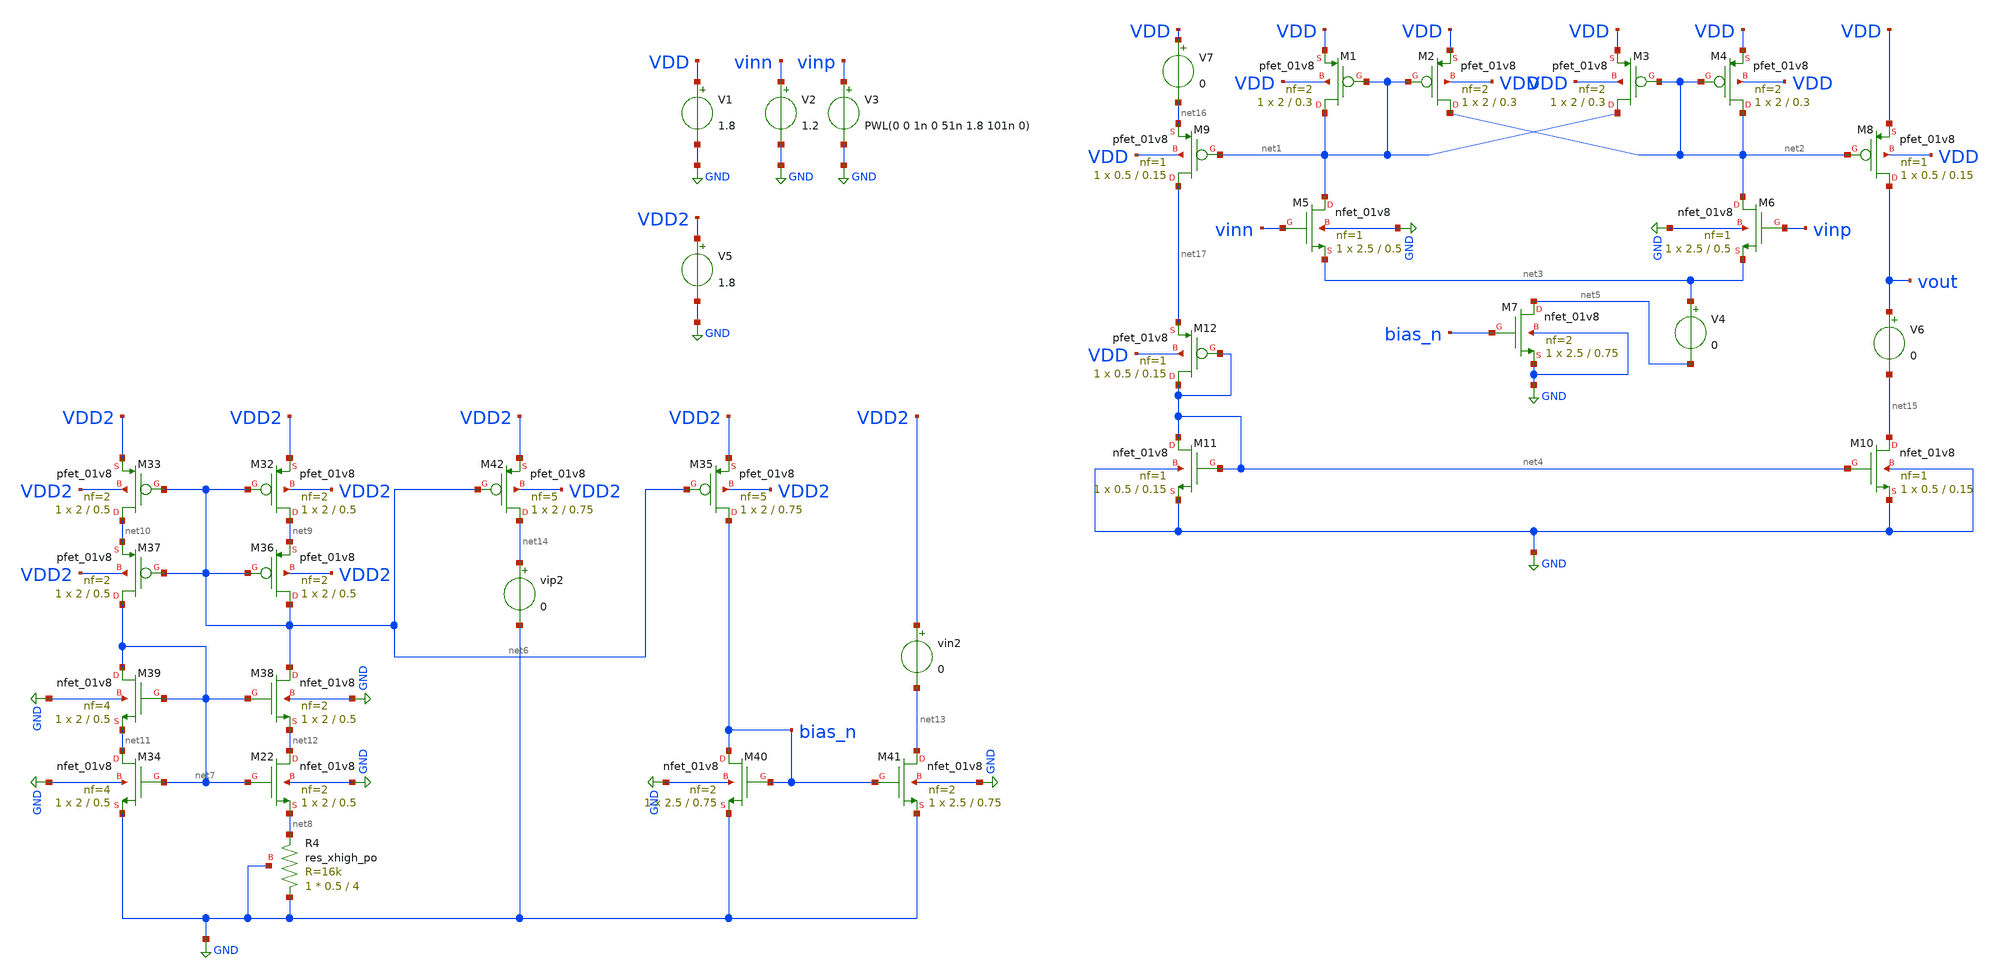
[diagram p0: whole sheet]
** sch_path: schem/comp_n.sch
**.subckt comp_n
XM1 net1 net1 VDD VDD sky130_fd_pr__pfet_01v8 L=0.3 W=2 nf=2 ad='int((2 + 1)/2) * 2 / 2 * 0.29' as='int((2 + 2)/2) * 2 / 2 * 0.29'
+ pd='2*int((2 + 1)/2) * (2 / 2 + 0.29)' ps='2*int((2 + 2)/2) * (2 / 2 + 0.29)' nrd='0.29 / 2 ' nrs='0.29 / 2 '
+ sa=0 sb=0 sd=0 mult=1 m=1
XM2 net2 net1 VDD VDD sky130_fd_pr__pfet_01v8 L=0.3 W=2 nf=2 ad='int((2 + 1)/2) * 2 / 2 * 0.29' as='int((2 + 2)/2) * 2 / 2 * 0.29'
+ pd='2*int((2 + 1)/2) * (2 / 2 + 0.29)' ps='2*int((2 + 2)/2) * (2 / 2 + 0.29)' nrd='0.29 / 2 ' nrs='0.29 / 2 '
+ sa=0 sb=0 sd=0 mult=1 m=1
XM3 net1 net2 VDD VDD sky130_fd_pr__pfet_01v8 L=0.3 W=2 nf=2 ad='int((2 + 1)/2) * 2 / 2 * 0.29' as='int((2 + 2)/2) * 2 / 2 * 0.29'
+ pd='2*int((2 + 1)/2) * (2 / 2 + 0.29)' ps='2*int((2 + 2)/2) * (2 / 2 + 0.29)' nrd='0.29 / 2 ' nrs='0.29 / 2 '
+ sa=0 sb=0 sd=0 mult=1 m=1
XM4 net2 net2 VDD VDD sky130_fd_pr__pfet_01v8 L=0.3 W=2 nf=2 ad='int((2 + 1)/2) * 2 / 2 * 0.29' as='int((2 + 2)/2) * 2 / 2 * 0.29'
+ pd='2*int((2 + 1)/2) * (2 / 2 + 0.29)' ps='2*int((2 + 2)/2) * (2 / 2 + 0.29)' nrd='0.29 / 2 ' nrs='0.29 / 2 '
+ sa=0 sb=0 sd=0 mult=1 m=1
XM5 net1 vinn net3 GND sky130_fd_pr__nfet_01v8 L=0.5 W=2.5 nf=1 ad='int((1 + 1)/2) * 2.5 / 1 * 0.29'
+ as='int((1 + 2)/2) * 2.5 / 1 * 0.29' pd='2*int((1 + 1)/2) * (2.5 / 1 + 0.29)' ps='2*int((1 + 2)/2) * (2.5 / 1 + 0.29)'
+ nrd='0.29 / 2.5 ' nrs='0.29 / 2.5 ' sa=0 sb=0 sd=0 mult=1 m=1
XM6 net2 vinp net3 GND sky130_fd_pr__nfet_01v8 L=0.5 W=2.5 nf=1 ad='int((1 + 1)/2) * 2.5 / 1 * 0.29'
+ as='int((1 + 2)/2) * 2.5 / 1 * 0.29' pd='2*int((1 + 1)/2) * (2.5 / 1 + 0.29)' ps='2*int((1 + 2)/2) * (2.5 / 1 + 0.29)'
+ nrd='0.29 / 2.5 ' nrs='0.29 / 2.5 ' sa=0 sb=0 sd=0 mult=1 m=1
XM7 net5 bias_n GND GND sky130_fd_pr__nfet_01v8 L=0.75 W=2.5 nf=2 ad='int((2 + 1)/2) * 2.5 / 2 * 0.29'
+ as='int((2 + 2)/2) * 2.5 / 2 * 0.29' pd='2*int((2 + 1)/2) * (2.5 / 2 + 0.29)' ps='2*int((2 + 2)/2) * (2.5 / 2 + 0.29)'
+ nrd='0.29 / 2.5 ' nrs='0.29 / 2.5 ' sa=0 sb=0 sd=0 mult=1 m=1
XM8 vout net2 VDD VDD sky130_fd_pr__pfet_01v8 L=0.15 W=0.5 nf=1 ad='int((1 + 1)/2) * 0.5 / 1 * 0.29'
+ as='int((1 + 2)/2) * 0.5 / 1 * 0.29' pd='2*int((1 + 1)/2) * (0.5 / 1 + 0.29)' ps='2*int((1 + 2)/2) * (0.5 / 1 + 0.29)'
+ nrd='0.29 / 0.5 ' nrs='0.29 / 0.5 ' sa=0 sb=0 sd=0 mult=1 m=1
XM9 net17 net1 net16 VDD sky130_fd_pr__pfet_01v8 L=0.15 W=0.5 nf=1 ad='int((1 + 1)/2) * 0.5 / 1 * 0.29'
+ as='int((1 + 2)/2) * 0.5 / 1 * 0.29' pd='2*int((1 + 1)/2) * (0.5 / 1 + 0.29)' ps='2*int((1 + 2)/2) * (0.5 / 1 + 0.29)'
+ nrd='0.29 / 0.5 ' nrs='0.29 / 0.5 ' sa=0 sb=0 sd=0 mult=1 m=1
XM10 net15 net4 GND GND sky130_fd_pr__nfet_01v8 L=0.15 W=0.5 nf=1 ad='int((1 + 1)/2) * 0.5 / 1 * 0.29'
+ as='int((1 + 2)/2) * 0.5 / 1 * 0.29' pd='2*int((1 + 1)/2) * (0.5 / 1 + 0.29)' ps='2*int((1 + 2)/2) * (0.5 / 1 + 0.29)'
+ nrd='0.29 / 0.5 ' nrs='0.29 / 0.5 ' sa=0 sb=0 sd=0 mult=1 m=1
XM11 net4 net4 GND GND sky130_fd_pr__nfet_01v8 L=0.15 W=0.5 nf=1 ad='int((1 + 1)/2) * 0.5 / 1 * 0.29'
+ as='int((1 + 2)/2) * 0.5 / 1 * 0.29' pd='2*int((1 + 1)/2) * (0.5 / 1 + 0.29)' ps='2*int((1 + 2)/2) * (0.5 / 1 + 0.29)'
+ nrd='0.29 / 0.5 ' nrs='0.29 / 0.5 ' sa=0 sb=0 sd=0 mult=1 m=1
V1 VDD GND 1.8
V2 vinn GND 1.2
V3 vinp GND PWL(0 0 1n 0 51n 1.8 101n 0)
V4 net3 net5 0
XM22 net12 net7 net8 GND sky130_fd_pr__nfet_01v8 L=0.5 W=2 nf=2 ad='int((2 + 1)/2) * 2 / 2 * 0.29' as='int((2 + 2)/2) * 2 / 2 * 0.29'
+ pd='2*int((2 + 1)/2) * (2 / 2 + 0.29)' ps='2*int((2 + 2)/2) * (2 / 2 + 0.29)' nrd='0.29 / 2 ' nrs='0.29 / 2 '
+ sa=0 sb=0 sd=0 mult=1 m=1
XM32 net9 net6 VDD2 VDD2 sky130_fd_pr__pfet_01v8 L=0.5 W=2 nf=2 ad='int((2 + 1)/2) * 2 / 2 * 0.29' as='int((2 + 2)/2) * 2 / 2 * 0.29'
+ pd='2*int((2 + 1)/2) * (2 / 2 + 0.29)' ps='2*int((2 + 2)/2) * (2 / 2 + 0.29)' nrd='0.29 / 2 ' nrs='0.29 / 2 '
+ sa=0 sb=0 sd=0 mult=1 m=1
XM33 net10 net6 VDD2 VDD2 sky130_fd_pr__pfet_01v8 L=0.5 W=2 nf=2 ad='int((2 + 1)/2) * 2 / 2 * 0.29' as='int((2 + 2)/2) * 2 / 2 * 0.29'
+ pd='2*int((2 + 1)/2) * (2 / 2 + 0.29)' ps='2*int((2 + 2)/2) * (2 / 2 + 0.29)' nrd='0.29 / 2 ' nrs='0.29 / 2 '
+ sa=0 sb=0 sd=0 mult=1 m=1
XM34 net11 net7 GND GND sky130_fd_pr__nfet_01v8 L=0.5 W=2 nf=4 ad='int((4 + 1)/2) * 2 / 4 * 0.29' as='int((4 + 2)/2) * 2 / 4 * 0.29'
+ pd='2*int((4 + 1)/2) * (2 / 4 + 0.29)' ps='2*int((4 + 2)/2) * (2 / 4 + 0.29)' nrd='0.29 / 2 ' nrs='0.29 / 2 '
+ sa=0 sb=0 sd=0 mult=1 m=1
XR4 GND net8 GND sky130_fd_pr__res_xhigh_po W=0.5 L=4 mult=1 m=1
XM35 bias_n net6 VDD2 VDD2 sky130_fd_pr__pfet_01v8 L=0.75 W=2 nf=5 ad='int((5 + 1)/2) * 2 / 5 * 0.29'
+ as='int((5 + 2)/2) * 2 / 5 * 0.29' pd='2*int((5 + 1)/2) * (2 / 5 + 0.29)' ps='2*int((5 + 2)/2) * (2 / 5 + 0.29)'
+ nrd='0.29 / 2 ' nrs='0.29 / 2 ' sa=0 sb=0 sd=0 mult=1 m=1
XM36 net6 net6 net9 VDD2 sky130_fd_pr__pfet_01v8 L=0.5 W=2 nf=2 ad='int((2 + 1)/2) * 2 / 2 * 0.29' as='int((2 + 2)/2) * 2 / 2 * 0.29'
+ pd='2*int((2 + 1)/2) * (2 / 2 + 0.29)' ps='2*int((2 + 2)/2) * (2 / 2 + 0.29)' nrd='0.29 / 2 ' nrs='0.29 / 2 '
+ sa=0 sb=0 sd=0 mult=1 m=1
XM37 net7 net6 net10 VDD2 sky130_fd_pr__pfet_01v8 L=0.5 W=2 nf=2 ad='int((2 + 1)/2) * 2 / 2 * 0.29' as='int((2 + 2)/2) * 2 / 2 * 0.29'
+ pd='2*int((2 + 1)/2) * (2 / 2 + 0.29)' ps='2*int((2 + 2)/2) * (2 / 2 + 0.29)' nrd='0.29 / 2 ' nrs='0.29 / 2 '
+ sa=0 sb=0 sd=0 mult=1 m=1
XM38 net6 net7 net12 GND sky130_fd_pr__nfet_01v8 L=0.5 W=2 nf=2 ad='int((2 + 1)/2) * 2 / 2 * 0.29' as='int((2 + 2)/2) * 2 / 2 * 0.29'
+ pd='2*int((2 + 1)/2) * (2 / 2 + 0.29)' ps='2*int((2 + 2)/2) * (2 / 2 + 0.29)' nrd='0.29 / 2 ' nrs='0.29 / 2 '
+ sa=0 sb=0 sd=0 mult=1 m=1
XM39 net7 net7 net11 GND sky130_fd_pr__nfet_01v8 L=0.5 W=2 nf=4 ad='int((4 + 1)/2) * 2 / 4 * 0.29' as='int((4 + 2)/2) * 2 / 4 * 0.29'
+ pd='2*int((4 + 1)/2) * (2 / 4 + 0.29)' ps='2*int((4 + 2)/2) * (2 / 4 + 0.29)' nrd='0.29 / 2 ' nrs='0.29 / 2 '
+ sa=0 sb=0 sd=0 mult=1 m=1
XM40 bias_n bias_n GND GND sky130_fd_pr__nfet_01v8 L=0.75 W=2.5 nf=2 ad='int((2 + 1)/2) * 2.5 / 2 * 0.29'
+ as='int((2 + 2)/2) * 2.5 / 2 * 0.29' pd='2*int((2 + 1)/2) * (2.5 / 2 + 0.29)' ps='2*int((2 + 2)/2) * (2.5 / 2 + 0.29)'
+ nrd='0.29 / 2.5 ' nrs='0.29 / 2.5 ' sa=0 sb=0 sd=0 mult=1 m=1
XM41 net13 bias_n GND GND sky130_fd_pr__nfet_01v8 L=0.75 W=2.5 nf=2 ad='int((2 + 1)/2) * 2.5 / 2 * 0.29'
+ as='int((2 + 2)/2) * 2.5 / 2 * 0.29' pd='2*int((2 + 1)/2) * (2.5 / 2 + 0.29)' ps='2*int((2 + 2)/2) * (2.5 / 2 + 0.29)'
+ nrd='0.29 / 2.5 ' nrs='0.29 / 2.5 ' sa=0 sb=0 sd=0 mult=1 m=1
vin2 VDD2 net13 0
XM42 net14 net6 VDD2 VDD2 sky130_fd_pr__pfet_01v8 L=0.75 W=2 nf=5 ad='int((5 + 1)/2) * 2 / 5 * 0.29'
+ as='int((5 + 2)/2) * 2 / 5 * 0.29' pd='2*int((5 + 1)/2) * (2 / 5 + 0.29)' ps='2*int((5 + 2)/2) * (2 / 5 + 0.29)'
+ nrd='0.29 / 2 ' nrs='0.29 / 2 ' sa=0 sb=0 sd=0 mult=1 m=1
vip2 net14 GND 0
V5 VDD2 GND 1.8
V6 vout net15 0
V7 VDD net16 0
XM12 net4 net4 net17 VDD sky130_fd_pr__pfet_01v8 L=0.15 W=0.5 nf=1 ad='int((1 + 1)/2) * 0.5 / 1 * 0.29'
+ as='int((1 + 2)/2) * 0.5 / 1 * 0.29' pd='2*int((1 + 1)/2) * (0.5 / 1 + 0.29)' ps='2*int((1 + 2)/2) * (0.5 / 1 + 0.29)'
+ nrd='0.29 / 0.5 ' nrs='0.29 / 0.5 ' sa=0 sb=0 sd=0 mult=1 m=1
**** begin user architecture code


.lib /usr/local/share/pdk/sky130A/libs.tech/ngspice/sky130.lib.spice tt

.tran 0.01n 101n
.save all

.control
    run
    plot vinn vinp vout
    plot abs(i(v4))
.endc

.end


**** end user architecture code
**.ends
.GLOBAL GND
.end
